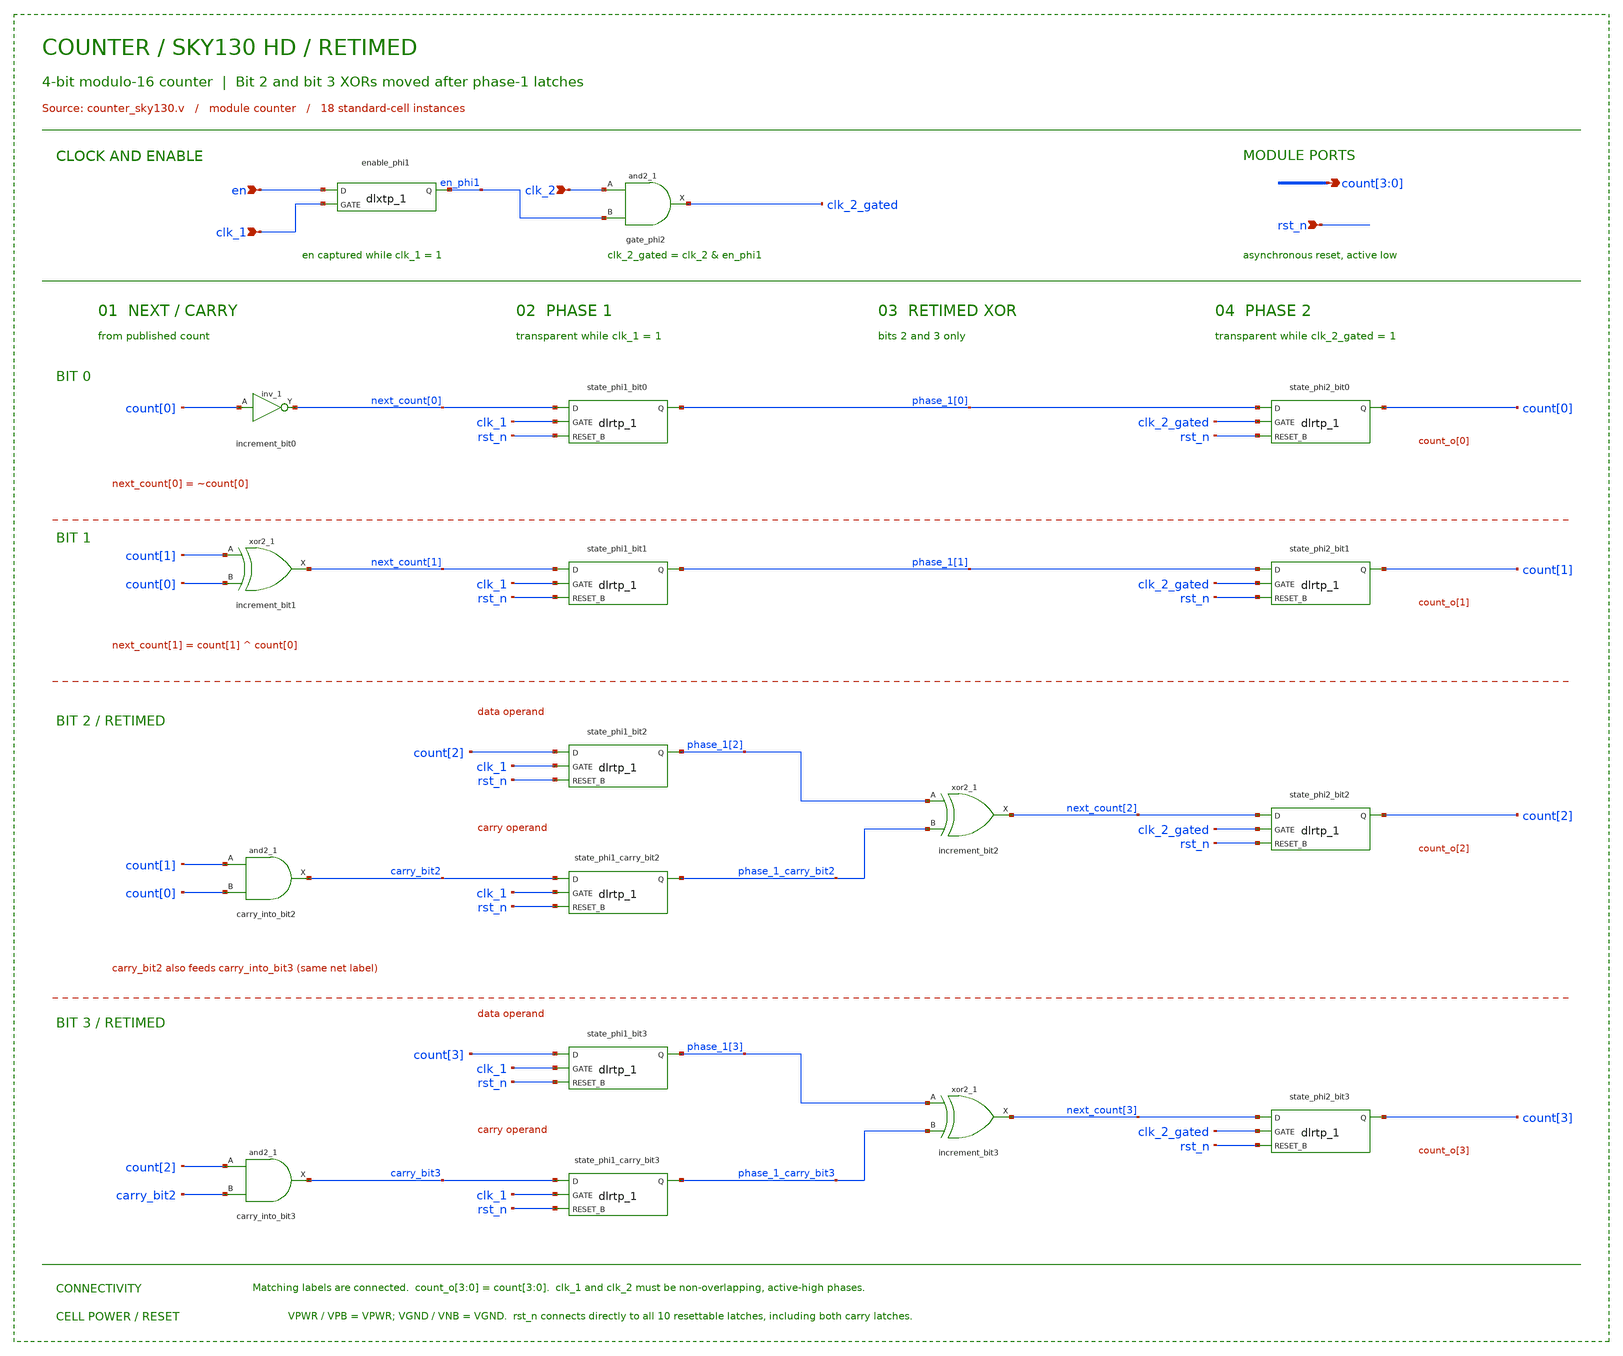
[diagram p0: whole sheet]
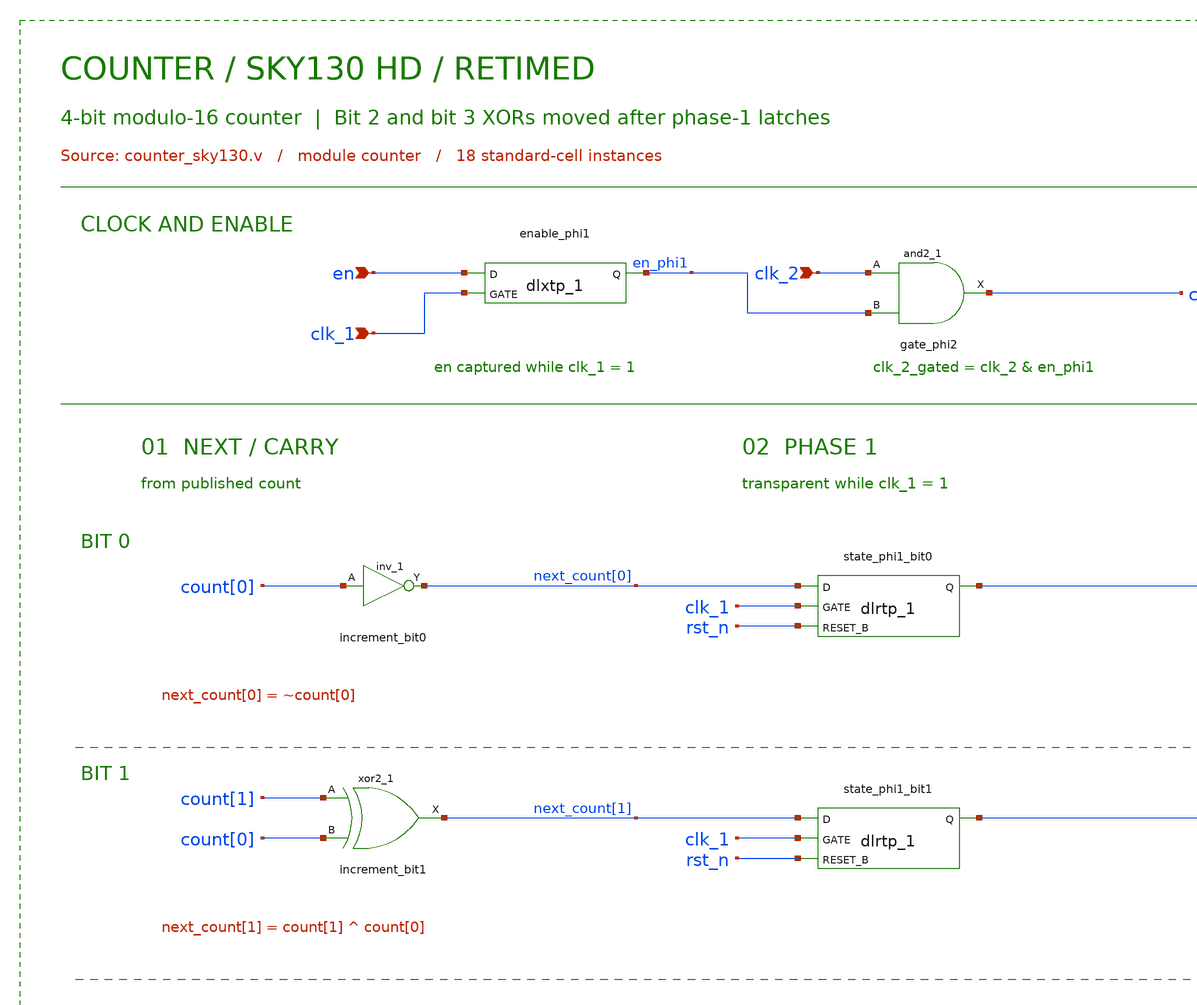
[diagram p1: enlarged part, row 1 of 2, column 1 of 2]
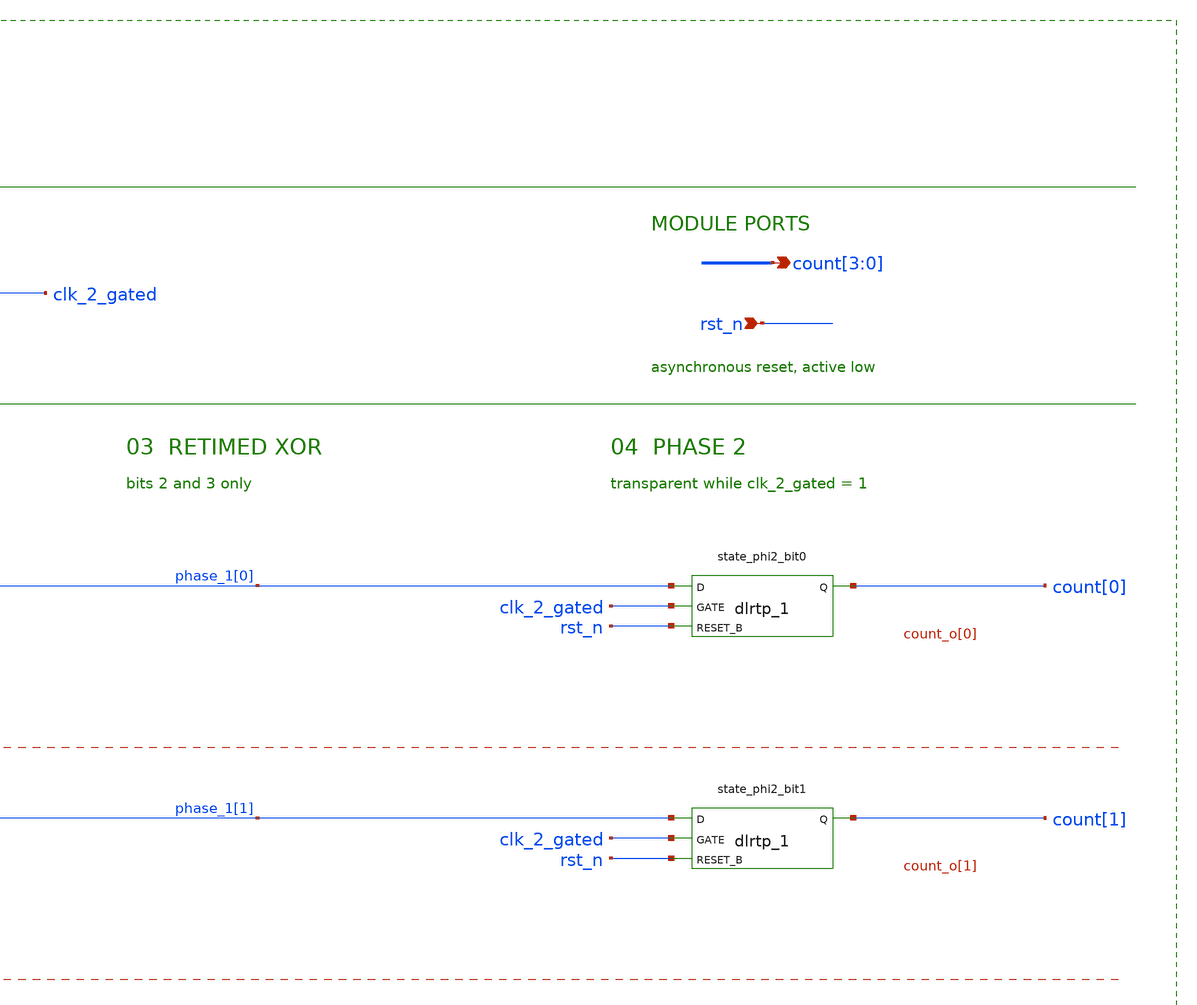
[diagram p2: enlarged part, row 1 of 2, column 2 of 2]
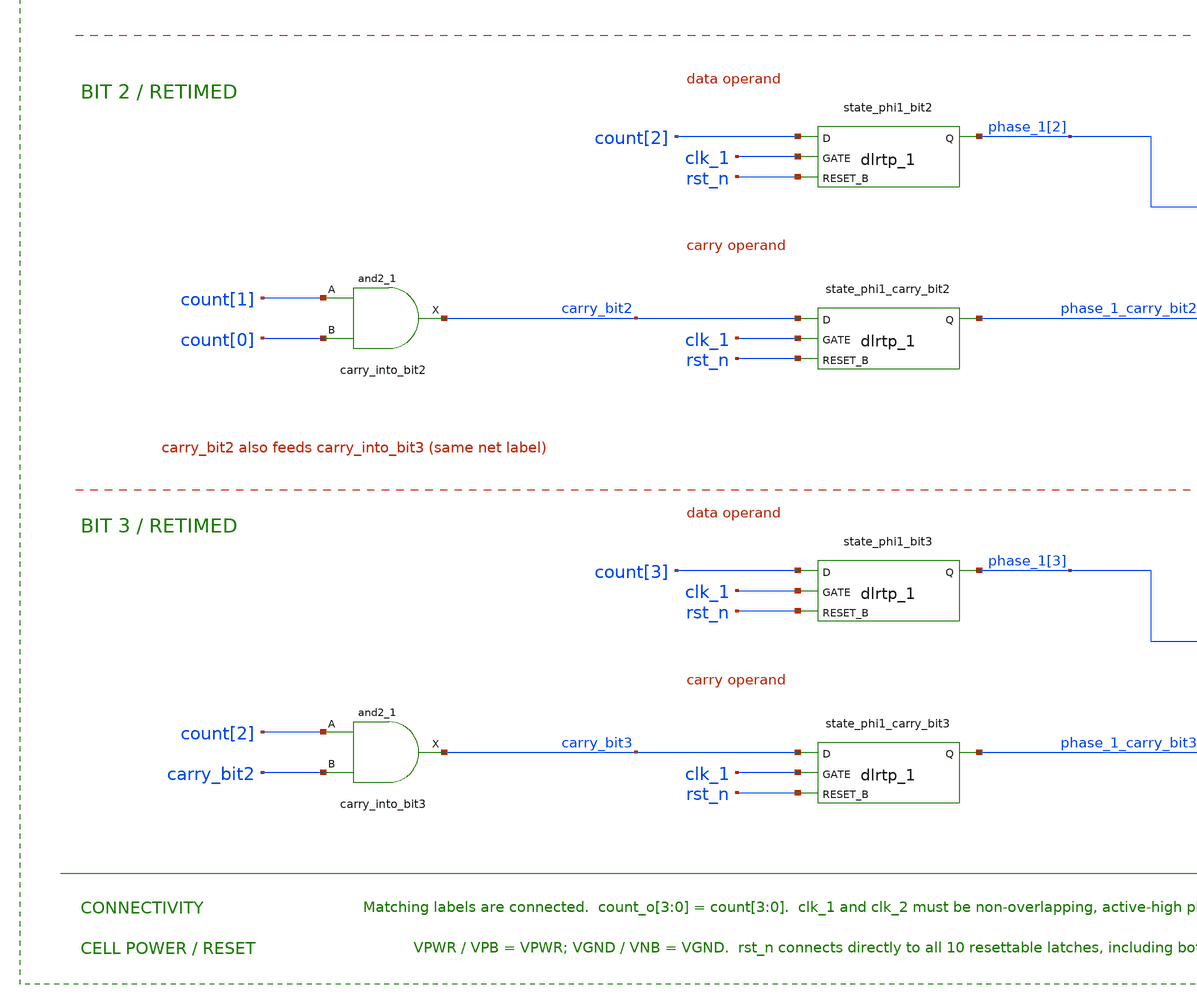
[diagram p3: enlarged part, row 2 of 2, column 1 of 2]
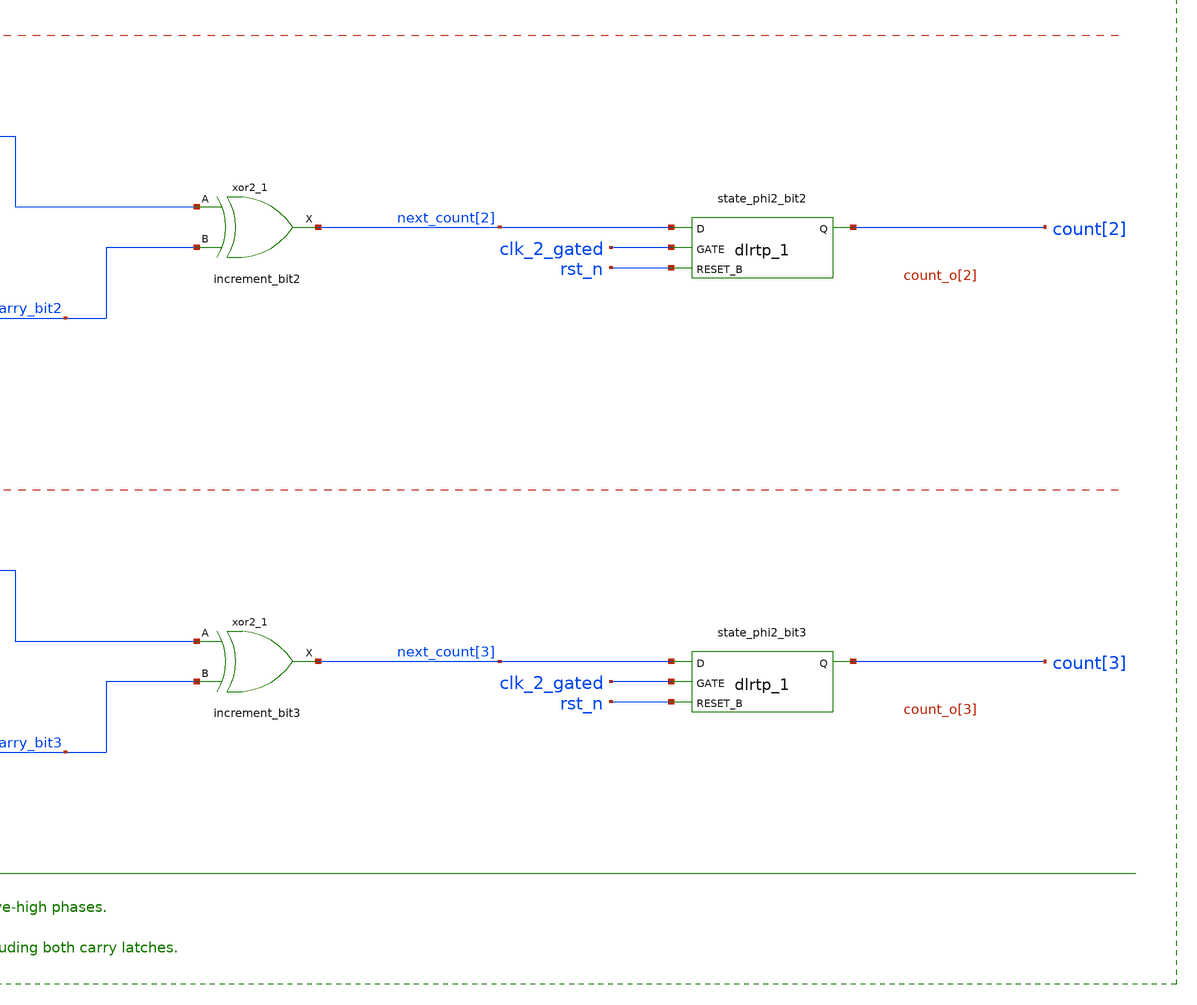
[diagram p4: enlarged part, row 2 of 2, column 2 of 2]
** sch_path: examples/counter/counter_latch_clock/counter_sky130.sch
**.subckt counter_sky130 en clk_1 clk_2 count[3],count[2],count[1],count[0] rst_n
*.ipin en
*.ipin clk_1
*.ipin clk_2
*.opin count[3],count[2],count[1],count[0]
*.ipin rst_n
enable_phi1 en clk_1 VGND VGND VPWR VPWR en_phi1 sky130_fd_sc_hd__dlxtp_1
gate_phi2 clk_2 en_phi1 VGND VGND VPWR VPWR clk_2_gated sky130_fd_sc_hd__and2_1
increment_bit0 count[0] VGND VGND VPWR VPWR next_count[0] sky130_fd_sc_hd__inv_1
state_phi1_bit0 next_count[0] clk_1 rst_n VGND VGND VPWR VPWR phase_1[0] sky130_fd_sc_hd__dlrtp_1
state_phi2_bit0 phase_1[0] clk_2_gated rst_n VGND VGND VPWR VPWR count[0] sky130_fd_sc_hd__dlrtp_1
increment_bit1 count[1] count[0] VGND VGND VPWR VPWR next_count[1] sky130_fd_sc_hd__xor2_1
state_phi1_bit1 next_count[1] clk_1 rst_n VGND VGND VPWR VPWR phase_1[1] sky130_fd_sc_hd__dlrtp_1
state_phi2_bit1 phase_1[1] clk_2_gated rst_n VGND VGND VPWR VPWR count[1] sky130_fd_sc_hd__dlrtp_1
state_phi1_bit2 count[2] clk_1 rst_n VGND VGND VPWR VPWR phase_1[2] sky130_fd_sc_hd__dlrtp_1
carry_into_bit2 count[1] count[0] VGND VGND VPWR VPWR carry_bit2 sky130_fd_sc_hd__and2_1
state_phi1_carry_bit2 carry_bit2 clk_1 rst_n VGND VGND VPWR VPWR phase_1_carry_bit2
+ sky130_fd_sc_hd__dlrtp_1
increment_bit2 phase_1[2] phase_1_carry_bit2 VGND VGND VPWR VPWR next_count[2]
+ sky130_fd_sc_hd__xor2_1
state_phi2_bit2 next_count[2] clk_2_gated rst_n VGND VGND VPWR VPWR count[2]
+ sky130_fd_sc_hd__dlrtp_1
state_phi1_bit3 count[3] clk_1 rst_n VGND VGND VPWR VPWR phase_1[3] sky130_fd_sc_hd__dlrtp_1
carry_into_bit3 count[2] carry_bit2 VGND VGND VPWR VPWR carry_bit3 sky130_fd_sc_hd__and2_1
state_phi1_carry_bit3 carry_bit3 clk_1 rst_n VGND VGND VPWR VPWR phase_1_carry_bit3
+ sky130_fd_sc_hd__dlrtp_1
increment_bit3 phase_1[3] phase_1_carry_bit3 VGND VGND VPWR VPWR next_count[3]
+ sky130_fd_sc_hd__xor2_1
state_phi2_bit3 next_count[3] clk_2_gated rst_n VGND VGND VPWR VPWR count[3]
+ sky130_fd_sc_hd__dlrtp_1
**.ends
.end
